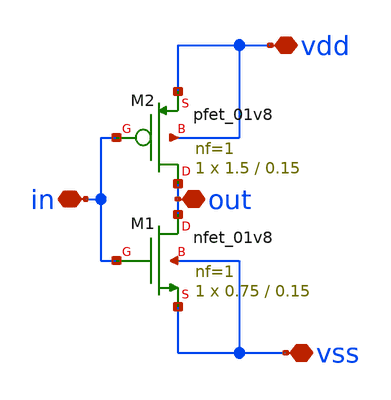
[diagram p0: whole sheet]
** sch_path: Todos los archivos para comparar/inverter.sch
**.subckt inverter in vdd vss out
*.iopin in
*.iopin vdd
*.iopin vss
*.iopin out
XM1 out in vss vss sky130_fd_pr__nfet_01v8 L=0.15 W=0.75 nf=1 ad='int((nf+1)/2) * W/nf * 0.29' as='int((nf+2)/2) * W/nf * 0.29'
+ pd='2*int((nf+1)/2) * (W/nf + 0.29)' ps='2*int((nf+2)/2) * (W/nf + 0.29)' nrd='0.29 / W' nrs='0.29 / W'
+ sa=0 sb=0 sd=0 mult=1 m=1
XM2 out in vdd vdd sky130_fd_pr__pfet_01v8 L=0.15 W=1.5 nf=1 ad='int((nf+1)/2) * W/nf * 0.29' as='int((nf+2)/2) * W/nf * 0.29'
+ pd='2*int((nf+1)/2) * (W/nf + 0.29)' ps='2*int((nf+2)/2) * (W/nf + 0.29)' nrd='0.29 / W' nrs='0.29 / W'
+ sa=0 sb=0 sd=0 mult=1 m=1
**.ends
.end
